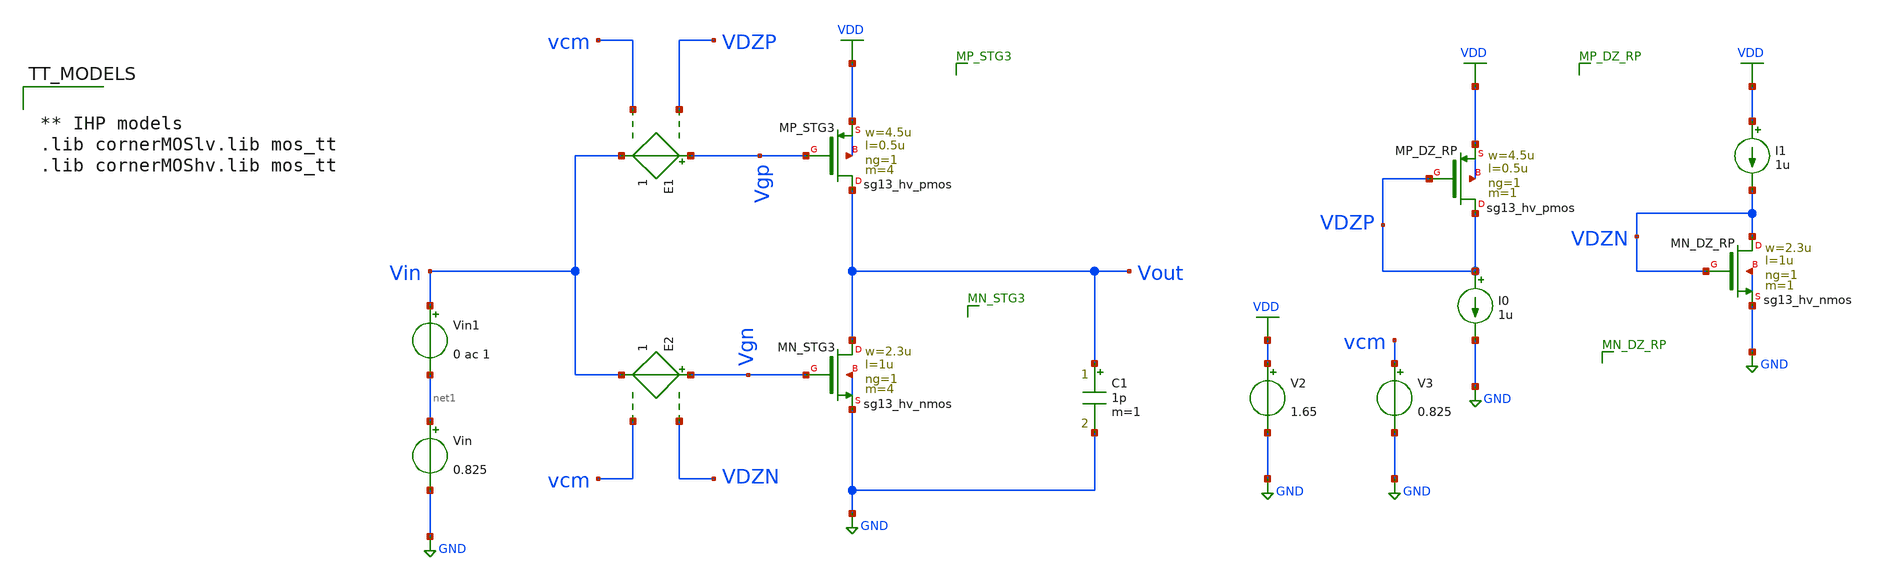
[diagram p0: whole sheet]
** sch_path: VLSI25/submitted_notebooks/Wrøngm/Schematics/INV_ota_gmid_try1_OPL.sch
**.subckt INV_ota_gmid_try1_OPL
Vin net1 GND 0.825
E1 Vgp Vin VDZP vcm 1
E2 Vgn Vin VDZN vcm 1
I0 VDZP GND 1u
I1 VDD VDZN 1u
V2 VDD GND 1.65
V3 vcm GND 0.825
XMP_STG3 Vout Vgp VDD VDD sg13_hv_pmos w=4.5u l=0.5u ng=1 m=4 mm_ok=1
XMP_DZ_RP VDZP VDZP VDD VDD sg13_hv_pmos w=4.5u l=0.5u ng=1 m=1 mm_ok=1
XMN_STG3 Vout Vgn GND GND sg13_hv_nmos w=2.3u l=1u ng=1 m=4 mm_ok=1
XMN_DZ_RP VDZN VDZN GND GND sg13_hv_nmos w=2.3u l=1u ng=1 m=1 mm_ok=1
C1 Vout GND 1p m=1
Vin1 Vin net1 0 ac 1
**** begin user architecture code


** IHP models
.lib cornerMOSlv.lib mos_tt
.lib cornerMOShv.lib mos_tt




.ic v(vout)=0.825 v(Vin)=0.825 v(vgn)=0.67213 v(vgp)=0.99954 v(Vx)=0.825
.option wnflag=1
.option savecurrents
.temp 27
.control
save all
write INV_ota_gmid_try1_OPL.raw
set appendwrite
op
write INV_ota_gmid_try1_OPL.raw
**dc V1 0 1.65 1m
**tran 1n 8u 0.1n
ac dec 20 1 1e10
plot vdb(vout)
**plot v(vout)
**plot v(vin)
**plot v(vgp)
**plot v(vgn)
**plot @n.xmp_stg3.nsg13_hv_pmos[ids] @n.xmn_stg3.nsg13_hv_nmos[ids]
**plot @n.xmp_stg3.nsg13_hv_pmos[ids]
**plot @n.xmn_stg3.nsg13_hv_nmos[ids]
**plot @c1[i]
.endc




.save @n.xmp_stg3.nsg13_hv_pmos[gm]
.save @n.xmp_stg3.nsg13_hv_pmos[gds]
.save @n.xmp_stg3.nsg13_hv_pmos[vth]
.save @n.xmp_stg3.nsg13_hv_pmos[vdss]
.save @n.xmp_stg3.nsg13_hv_pmos[cgg]
.save @n.xmp_stg3.nsg13_hv_pmos[cgsol]
.save @n.xmp_stg3.nsg13_hv_pmos[cgdol]
.save @n.xmp_dz_rp.nsg13_hv_pmos[gm]
.save @n.xmp_dz_rp.nsg13_hv_pmos[gds]
.save @n.xmp_dz_rp.nsg13_hv_pmos[vth]
.save @n.xmp_dz_rp.nsg13_hv_pmos[vdss]
.save @n.xmp_dz_rp.nsg13_hv_pmos[cgg]
.save @n.xmp_dz_rp.nsg13_hv_pmos[cgsol]
.save @n.xmp_dz_rp.nsg13_hv_pmos[cgdol]
.save @n.xmn_stg3.nsg13_hv_nmos[gm]
.save @n.xmn_stg3.nsg13_hv_nmos[gds]
.save @n.xmn_stg3.nsg13_hv_nmos[vth]
.save @n.xmn_stg3.nsg13_hv_nmos[vdss]
.save @n.xmn_stg3.nsg13_hv_nmos[cgg]
.save @n.xmn_stg3.nsg13_hv_nmos[cgsol]
.save @n.xmn_stg3.nsg13_hv_nmos[cgdol]
.save @n.xmn_dz_rp.nsg13_hv_nmos[gm]
.save @n.xmn_dz_rp.nsg13_hv_nmos[gds]
.save @n.xmn_dz_rp.nsg13_hv_nmos[vth]
.save @n.xmn_dz_rp.nsg13_hv_nmos[vdss]
.save @n.xmn_dz_rp.nsg13_hv_nmos[cgg]
.save @n.xmn_dz_rp.nsg13_hv_nmos[cgsol]
.save @n.xmn_dz_rp.nsg13_hv_nmos[cgdol]



**** end user architecture code
**.ends
.GLOBAL GND
.GLOBAL VDD
.end
